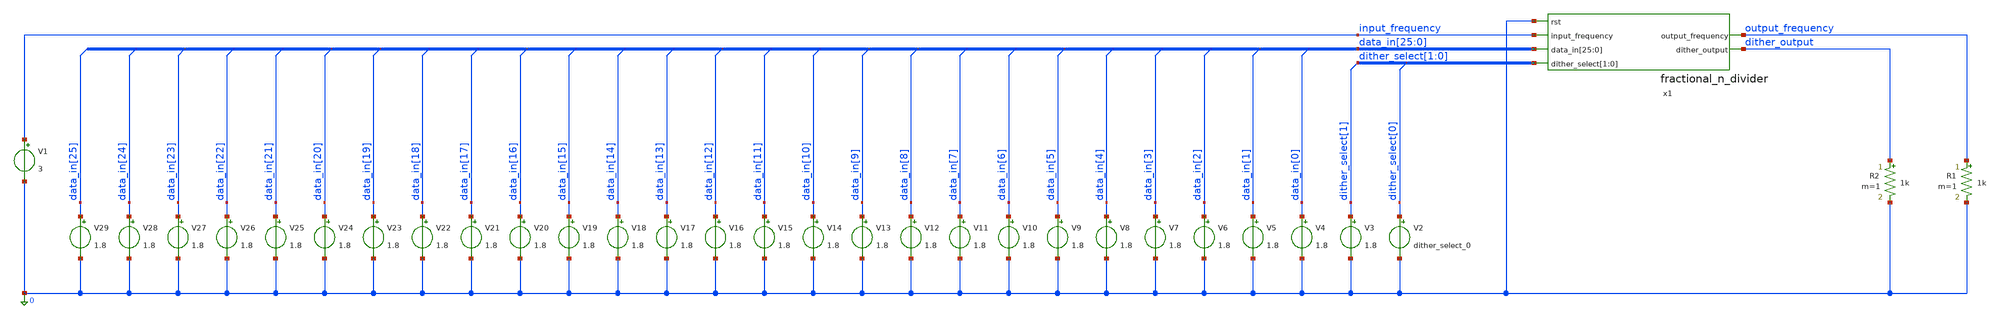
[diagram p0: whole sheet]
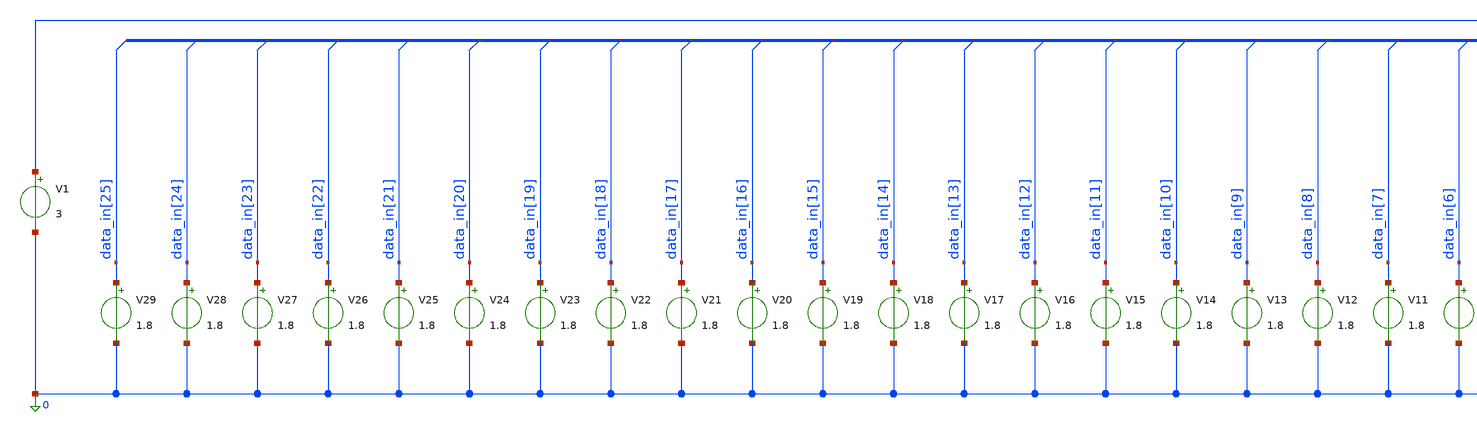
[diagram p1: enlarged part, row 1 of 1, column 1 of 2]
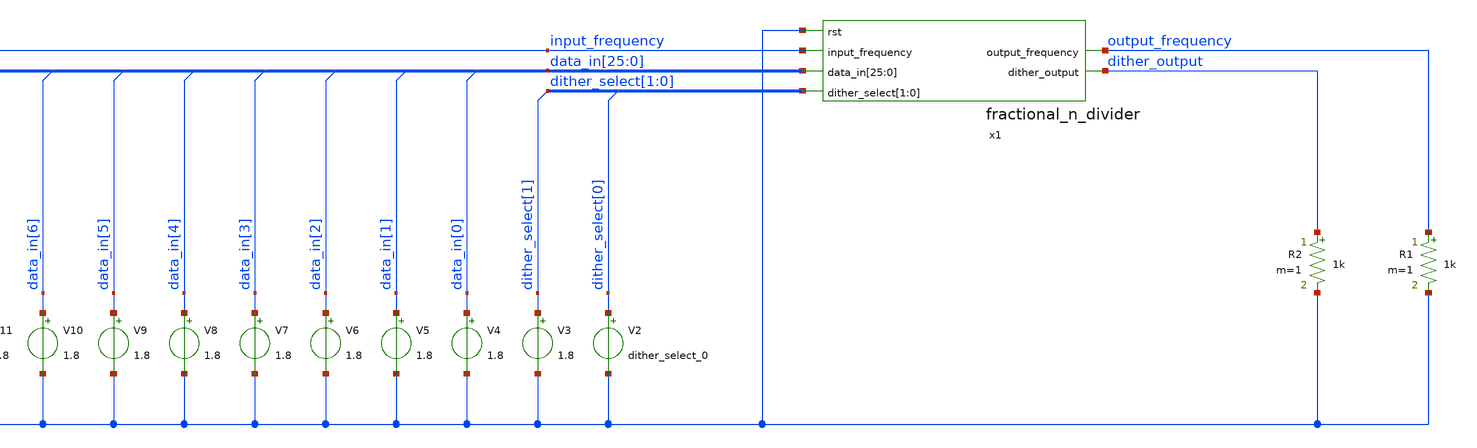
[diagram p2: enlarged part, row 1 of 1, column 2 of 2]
** sch_path: design/fractional_n_divider/tests/fractional_n_divider_tb.sch
**.subckt fractional_n_divider_tb
x1 0 output_frequency input_frequency data_in[25] data_in[24] data_in[23] data_in[22] data_in[21]
+ data_in[20] data_in[19] data_in[18] data_in[17] data_in[16] data_in[15] data_in[14] data_in[13] data_in[12]
+ data_in[11] data_in[10] data_in[9] data_in[8] data_in[7] data_in[6] data_in[5] data_in[4] data_in[3] data_in[2]
+ data_in[1] data_in[0] dither_output dither_select[1] dither_select[0] fractional_n_divider
V1 input_frequency 0 3
V2 dither_select[0] 0 dither_select_0
V3 dither_select[1] 0 1.8
V4 data_in[0] 0 1.8
V5 data_in[1] 0 1.8
R1 output_frequency 0 1k m=1
R2 dither_output 0 1k m=1
V6 data_in[2] 0 1.8
V7 data_in[3] 0 1.8
V8 data_in[4] 0 1.8
V9 data_in[5] 0 1.8
V10 data_in[6] 0 1.8
V11 data_in[7] 0 1.8
V12 data_in[8] 0 1.8
V13 data_in[9] 0 1.8
V14 data_in[10] 0 1.8
V15 data_in[11] 0 1.8
V16 data_in[12] 0 1.8
V17 data_in[13] 0 1.8
V18 data_in[14] 0 1.8
V19 data_in[15] 0 1.8
V20 data_in[16] 0 1.8
V21 data_in[17] 0 1.8
V22 data_in[18] 0 1.8
V23 data_in[19] 0 1.8
V24 data_in[20] 0 1.8
V25 data_in[21] 0 1.8
V26 data_in[22] 0 1.8
V27 data_in[23] 0 1.8
V28 data_in[24] 0 1.8
V29 data_in[25] 0 1.8
**** begin user architecture code


*.option PARHIER=LOCAL RUNLVL=6 post MODMONTE=1 warn maxwarns=400
*.option ITL4=20000 ITL5=0
* .option sampling_method = SRS
* .option method=gear

* simple transistor model
.MODEL cmosn NMOS LEVEL=1 VT0=0.7 KP=110U GAMMA=0.4 LAMBDA=0.04 PHI=0.7
.MODEL cmosp PMOS LEVEL=1 VT0=-0.7 KP=50U GAMMA=0.57 LAMBDA=0.05 PHI=0.8

* load design and library
.include /home/tom/repositories/amsat_txrx_ic/design/fractional_n_divider/yosys/prim_cells_cmos.mod

.temp 30
.tran  1e-9 1e-6 uic


**** end user architecture code
**.ends

* expanding   symbol:  fractional_n_divider/fractional_n_divider.sym # of pins=6
** sym_path: design/fractional_n_divider/fractional_n_divider.sym
** sch_path: design/fractional_n_divider/fractional_n_divider.sch
.subckt fractional_n_divider rst output_frequency input_frequency data_in[25] data_in[24]
+ data_in[23] data_in[22] data_in[21] data_in[20] data_in[19] data_in[18] data_in[17] data_in[16] data_in[15]
+ data_in[14] data_in[13] data_in[12] data_in[11] data_in[10] data_in[9] data_in[8] data_in[7] data_in[6]
+ data_in[5] data_in[4] data_in[3] data_in[2] data_in[1] data_in[0] dither_output dither_select[1]
+ dither_select[0]
*.ipin rst
*.ipin input_frequency
*.opin output_frequency
*.ipin
*+ data_in[25],data_in[24],data_in[23],data_in[22],data_in[21],data_in[20],data_in[19],data_in[18],data_in[17],data_in[16],data_in[15],data_in[14],data_in[13],data_in[12],data_in[11],data_in[10],data_in[9],data_in[8],data_in[7],data_in[6],data_in[5],data_in[4],data_in[3],data_in[2],data_in[1],data_in[0]
*.ipin dither_select[1],dither_select[0]
*.opin dither_output
.ends

.end
